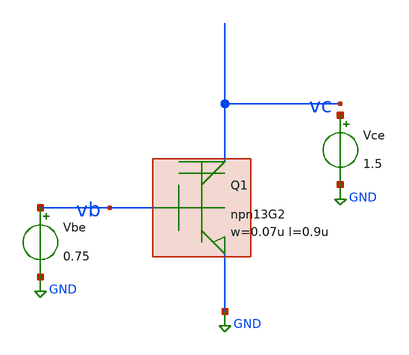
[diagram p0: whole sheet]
** sch_path: xschem/tb_npn13G2_dc.sch
**.subckt tb_npn13G2_dc
KQ1 npn13G2 w=0.07u l=0.9u nx=1 ny=1
Vbe vb GND 0.75
Vce net2 GND 1.5
**** begin user architecture code


.param temp=27
.dc Vce 0 3.3 0.01 Vbe 0.65 0.85 0.05
.save i(Vce) i(Vbe)


**** end user architecture code
**.ends
.GLOBAL GND
.end
